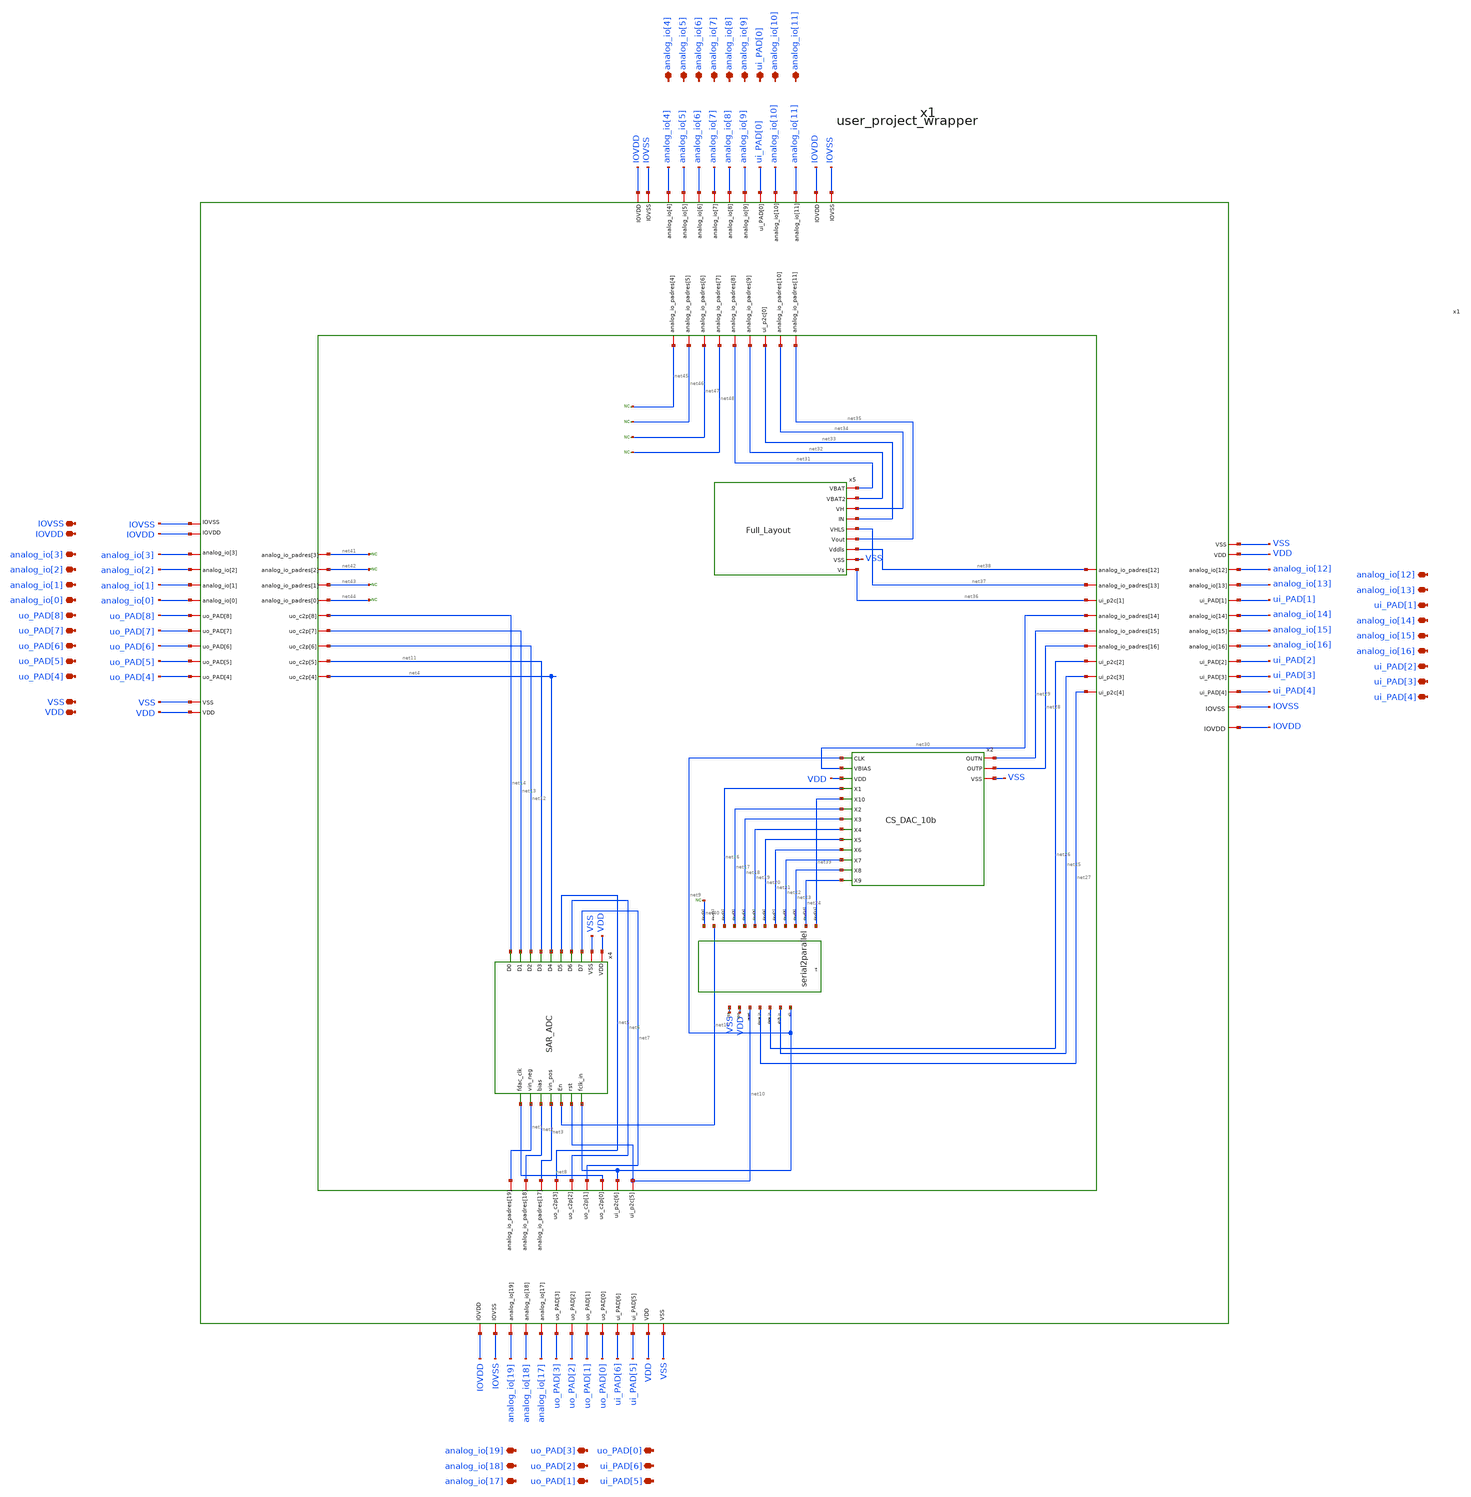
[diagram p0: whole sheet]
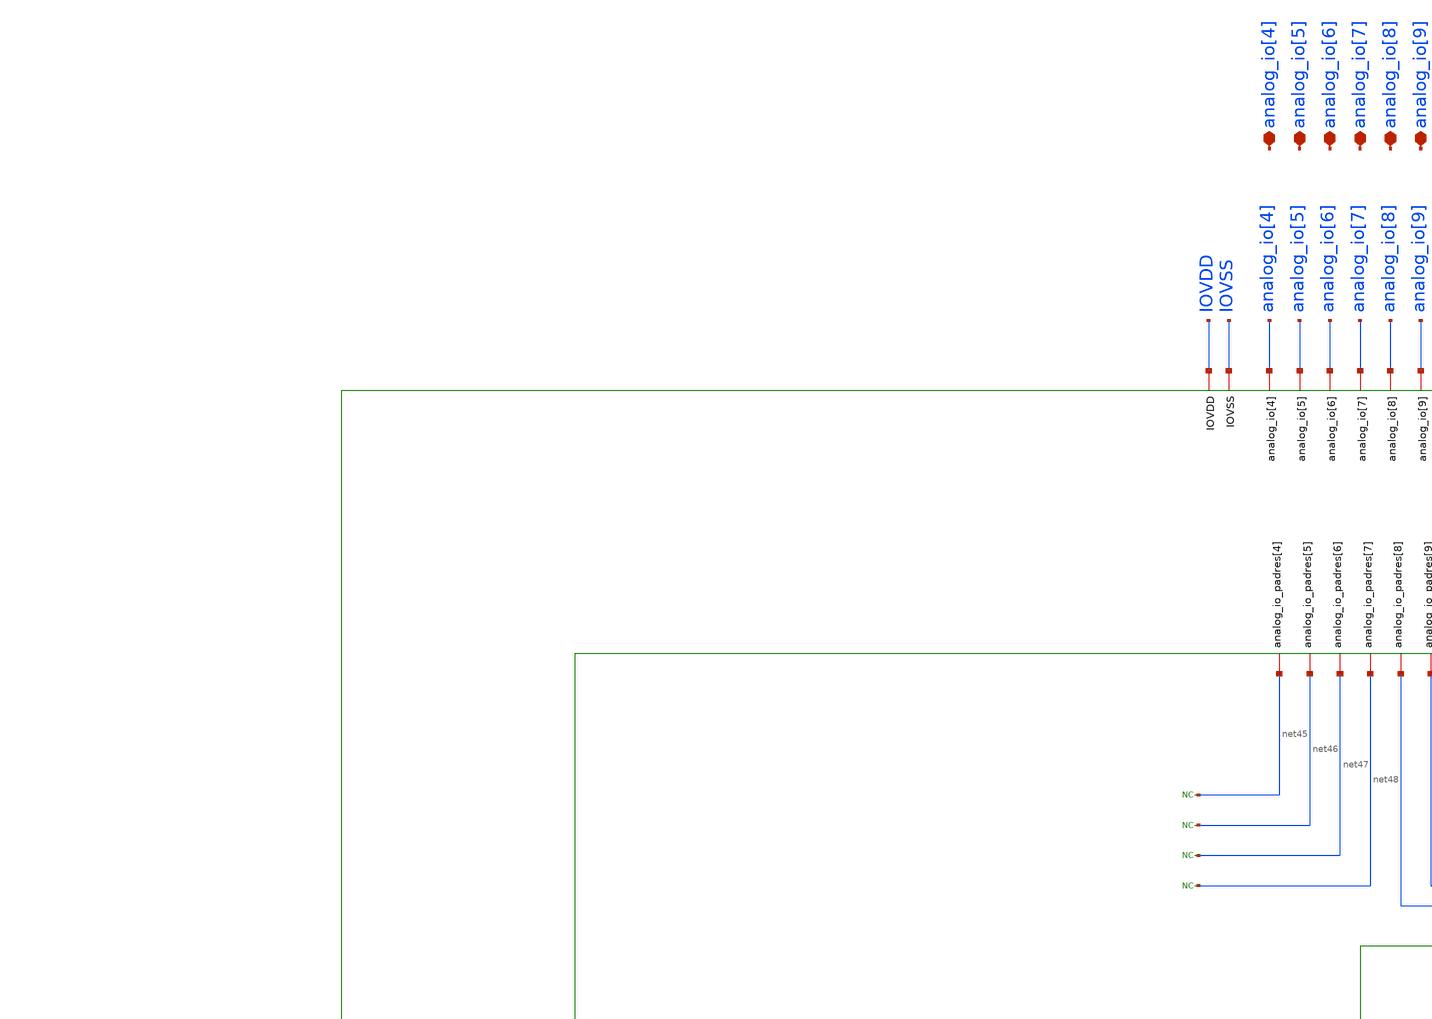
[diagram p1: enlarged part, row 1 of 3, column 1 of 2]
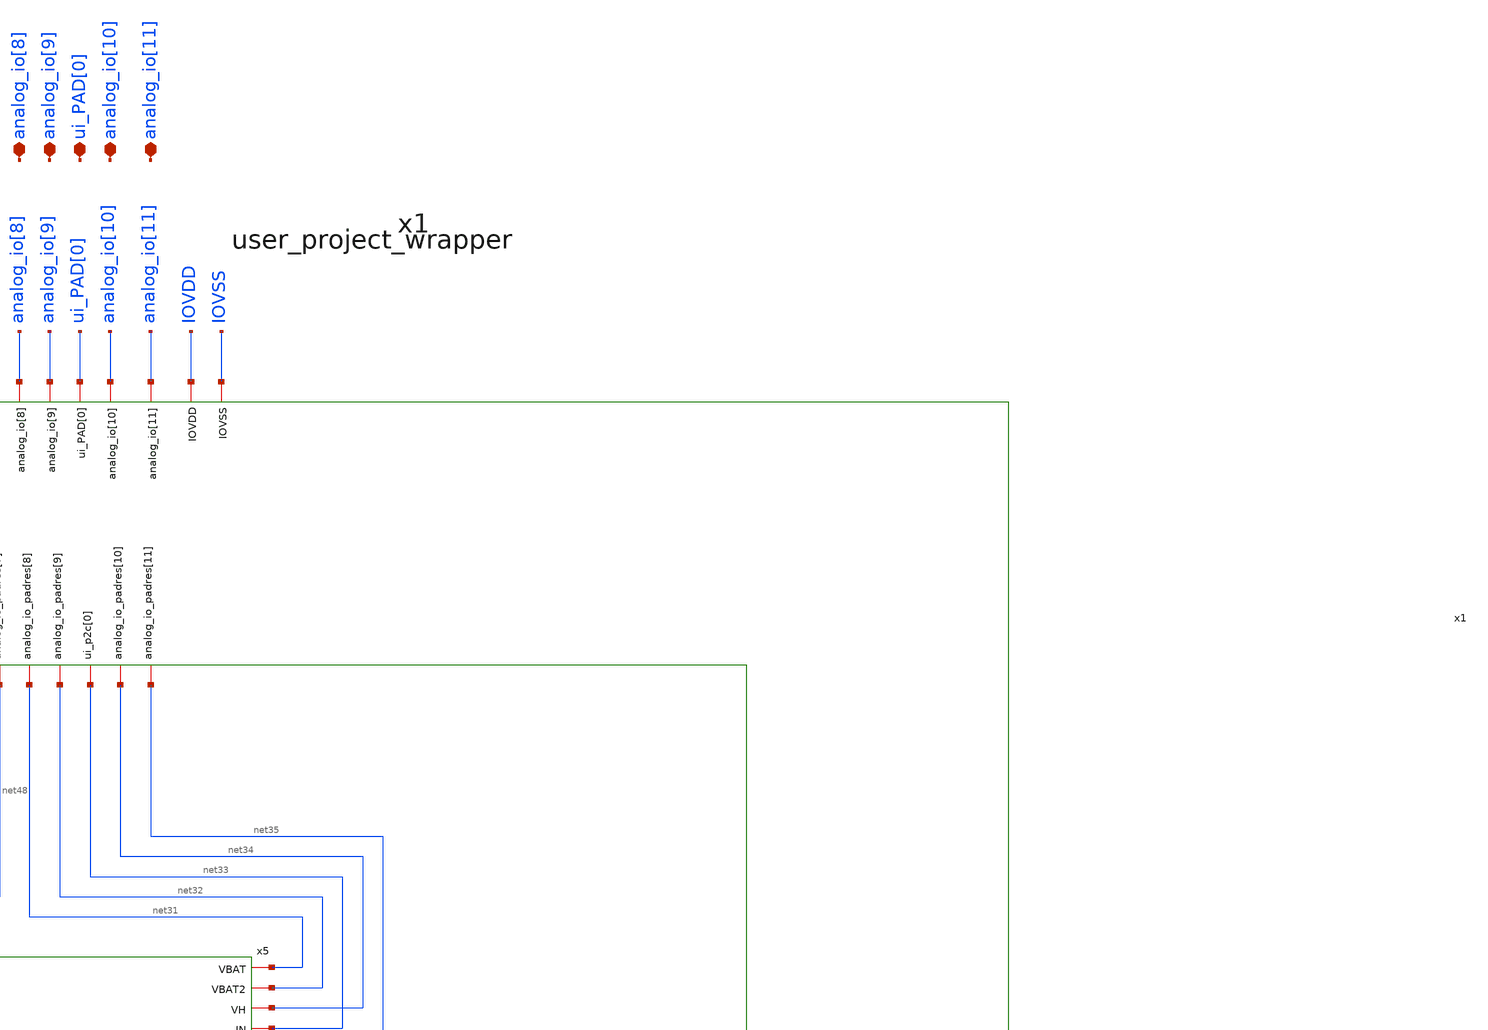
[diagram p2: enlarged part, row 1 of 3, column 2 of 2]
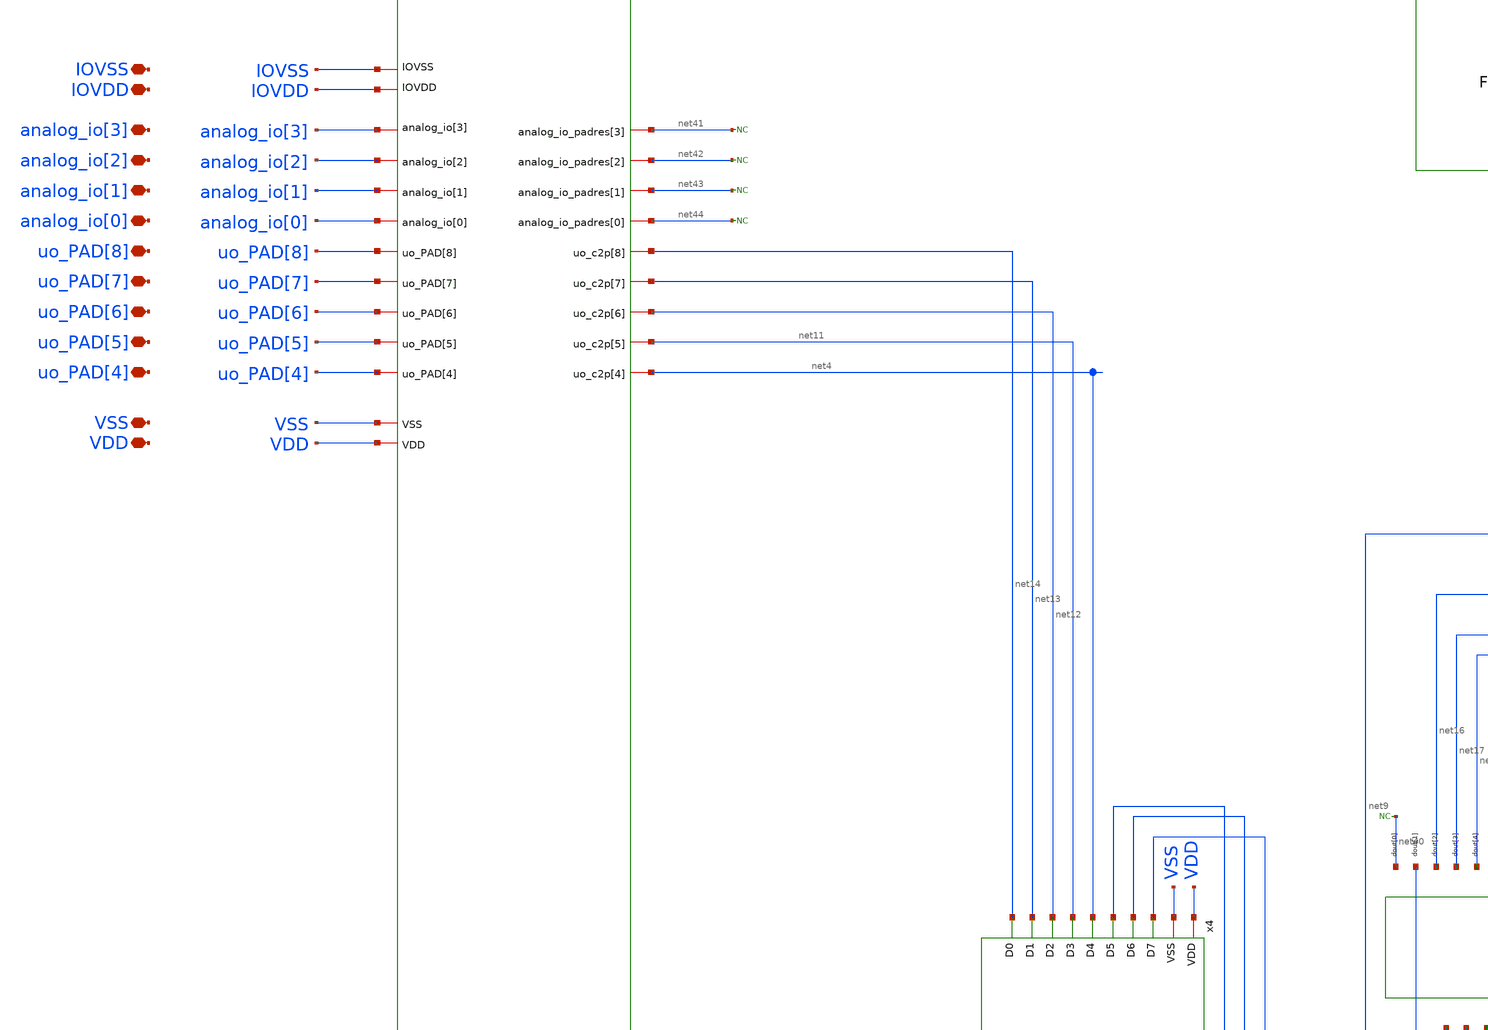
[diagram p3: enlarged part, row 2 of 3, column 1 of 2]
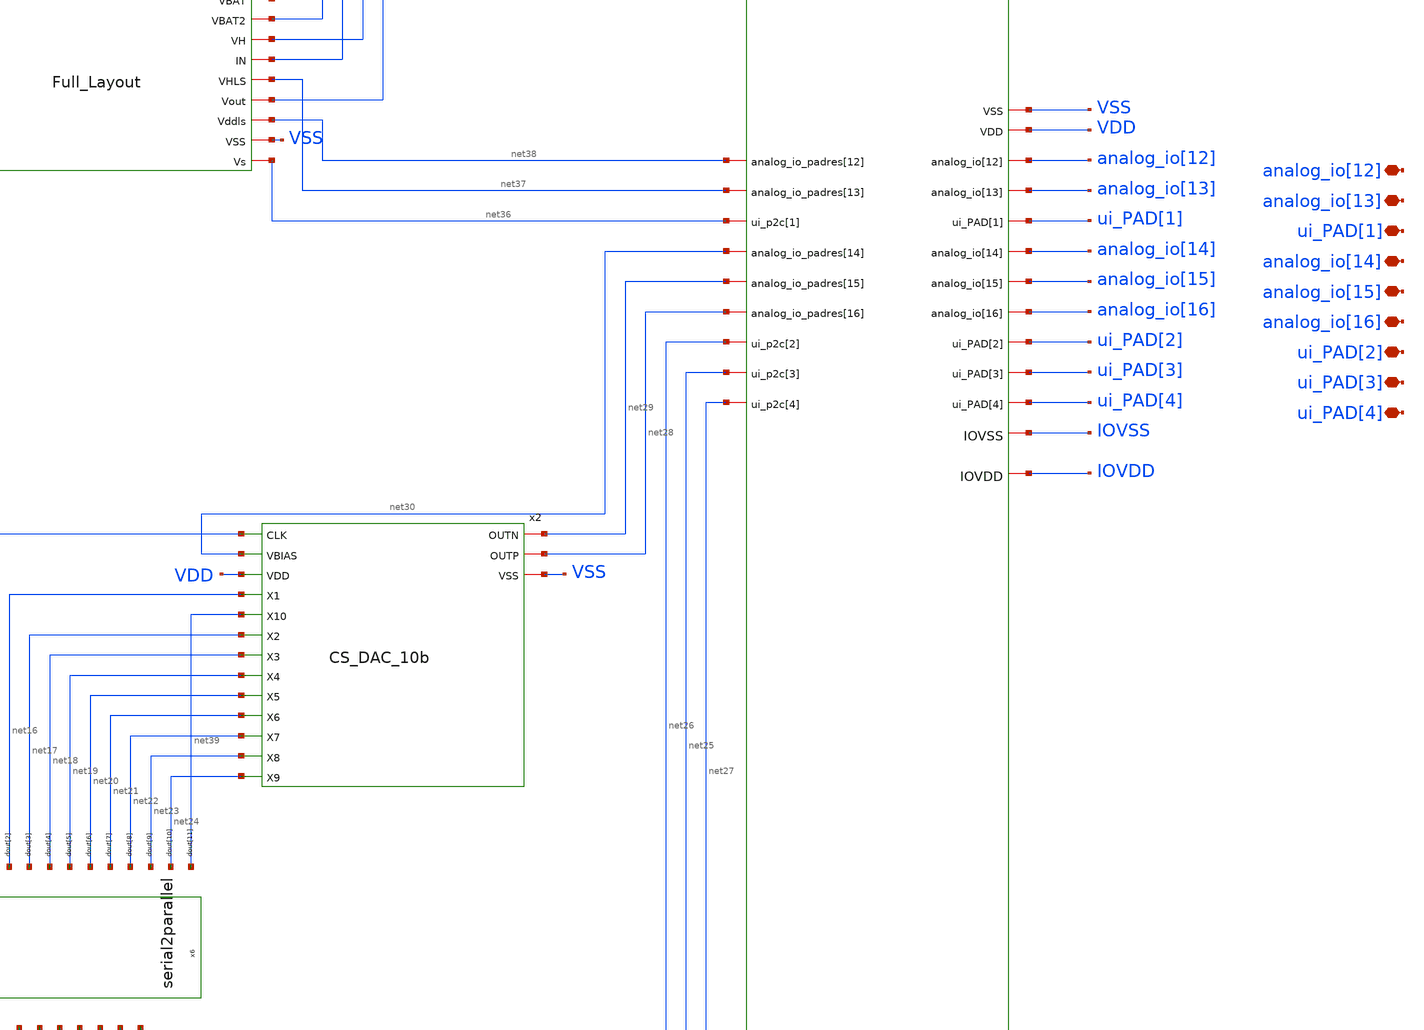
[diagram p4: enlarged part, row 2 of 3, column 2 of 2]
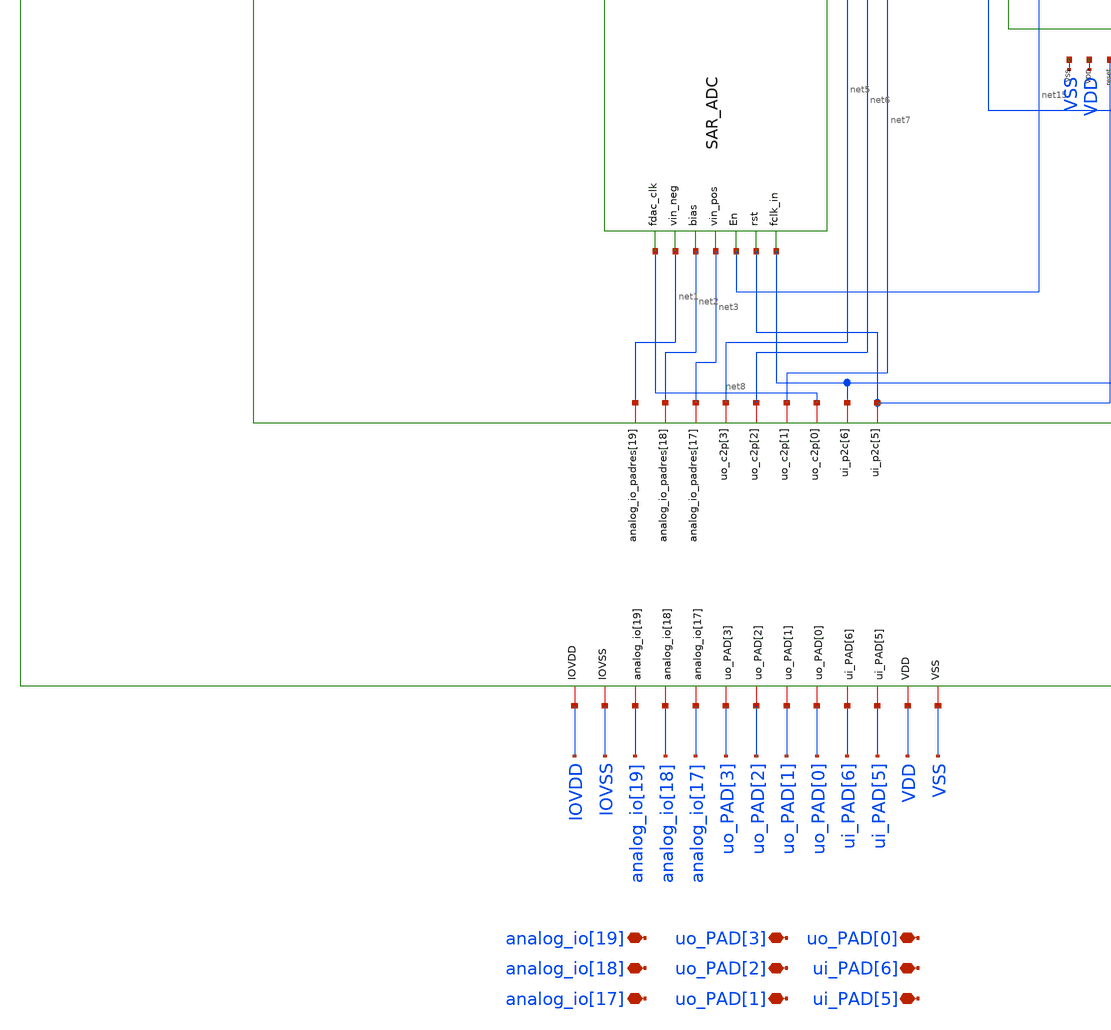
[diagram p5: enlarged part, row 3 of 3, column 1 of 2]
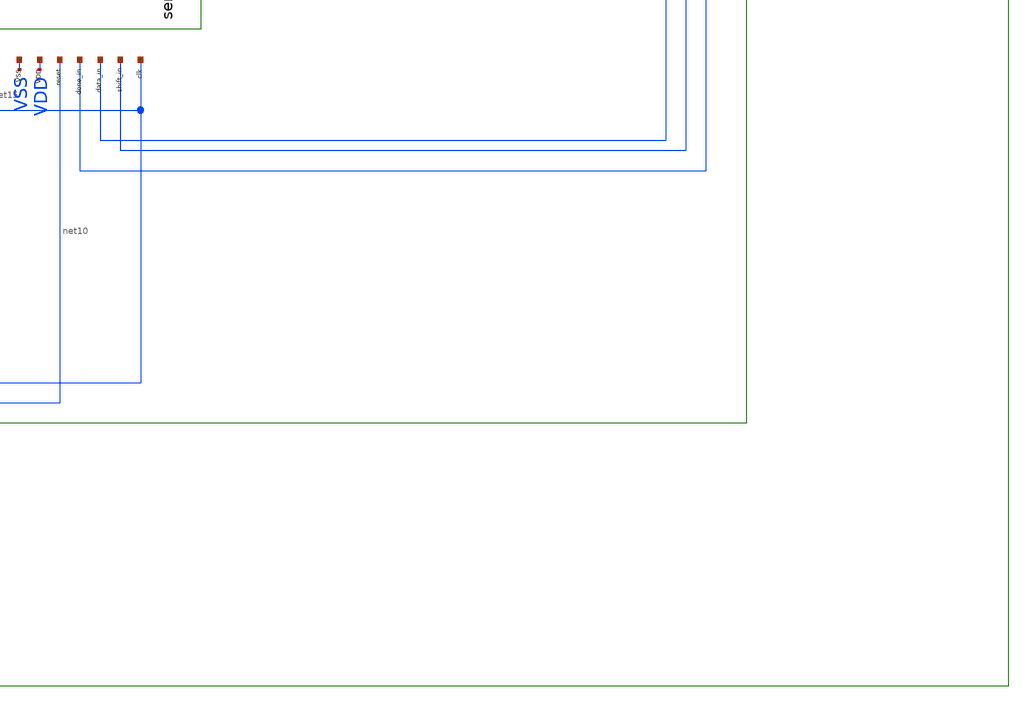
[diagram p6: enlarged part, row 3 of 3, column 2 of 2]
** sch_path: release/v.1.0.0/doc/team4_chip_top.sch
**.subckt team4_chip_top IOVSS IOVDD analog_io[3] analog_io[2] analog_io[1] analog_io[0] uo_PAD[8]
*+ uo_PAD[7] uo_PAD[6] uo_PAD[5] uo_PAD[4] VSS VDD analog_io[19] analog_io[18] analog_io[17] uo_PAD[3] uo_PAD[2]
*+ uo_PAD[1] uo_PAD[0] ui_PAD[6] ui_PAD[5] ui_PAD[4] ui_PAD[3] ui_PAD[2] analog_io[16] analog_io[15]
*+ analog_io[14] ui_PAD[1] analog_io[13] analog_io[12] analog_io[4] analog_io[5] analog_io[6] analog_io[7]
*+ analog_io[8] analog_io[9] ui_PAD[0] analog_io[10] analog_io[11]
*.iopin IOVSS
*.iopin IOVDD
*.iopin analog_io[3]
*.iopin analog_io[2]
*.iopin analog_io[1]
*.iopin analog_io[0]
*.iopin uo_PAD[8]
*.iopin uo_PAD[7]
*.iopin uo_PAD[6]
*.iopin uo_PAD[5]
*.iopin uo_PAD[4]
*.iopin VSS
*.iopin VDD
*.iopin analog_io[19]
*.iopin analog_io[18]
*.iopin analog_io[17]
*.iopin uo_PAD[3]
*.iopin uo_PAD[2]
*.iopin uo_PAD[1]
*.iopin uo_PAD[0]
*.iopin ui_PAD[6]
*.iopin ui_PAD[5]
*.iopin ui_PAD[4]
*.iopin ui_PAD[3]
*.iopin ui_PAD[2]
*.iopin analog_io[16]
*.iopin analog_io[15]
*.iopin analog_io[14]
*.iopin ui_PAD[1]
*.iopin analog_io[13]
*.iopin analog_io[12]
*.iopin analog_io[4]
*.iopin analog_io[5]
*.iopin analog_io[6]
*.iopin analog_io[7]
*.iopin analog_io[8]
*.iopin analog_io[9]
*.iopin ui_PAD[0]
*.iopin analog_io[10]
*.iopin analog_io[11]
x1 analog_io[8] analog_io[6] analog_io[11] ui_PAD[0] analog_io[10] analog_io[7] analog_io[9]
+ analog_io[4] analog_io[5] net45 net35 net46 net47 net33 net34 net48 net31 net32 net38 analog_io[3] analog_io[12]
+ net41 net37 analog_io[2] analog_io[13] net42 net36 analog_io[1] ui_PAD[1] net43 net30 analog_io[0]
+ analog_io[14] net44 net29 uo_PAD[8] analog_io[15] net28 uo_PAD[7] analog_io[16] net13 net26 uo_PAD[6] ui_PAD[2]
+ net12 net25 uo_PAD[5] ui_PAD[3] net11 net27 uo_PAD[4] ui_PAD[4] net4 net10 net9 net8 net7 net6 net5 net3
+ net2 net1 VSS VDD IOVDD IOVSS analog_io[19] analog_io[18] analog_io[17] uo_PAD[3] uo_PAD[2] uo_PAD[1]
+ uo_PAD[0] ui_PAD[6] ui_PAD[5] net14 user_project_wrapper
x5 net31 net32 net34 net33 net37 net35 net38 VSS net36 Full_Layout
x6 net9 net25 net26 net27 net10 VDD VSS net39 net24 net23 net22 net21 net20 net19 net18 net17 net16
+ net15 net40 serial2parallel
* noconn #net40
* noconn #net45
* noconn #net46
* noconn #net47
* noconn #net48
* noconn #net41
* noconn #net42
* noconn #net43
* noconn #net44
x4 net9 net10 net15 VDD VSS net8 net3 net2 net1 net7 net6 net5 net4 net11 net12 net13 net14 SAR_ADC
x2 net9 net29 net28 net30 VDD VSS net16 net39 net17 net18 net19 net20 net21 net22 net23 net24
+ CS_DAC_10b
**.ends
.end
